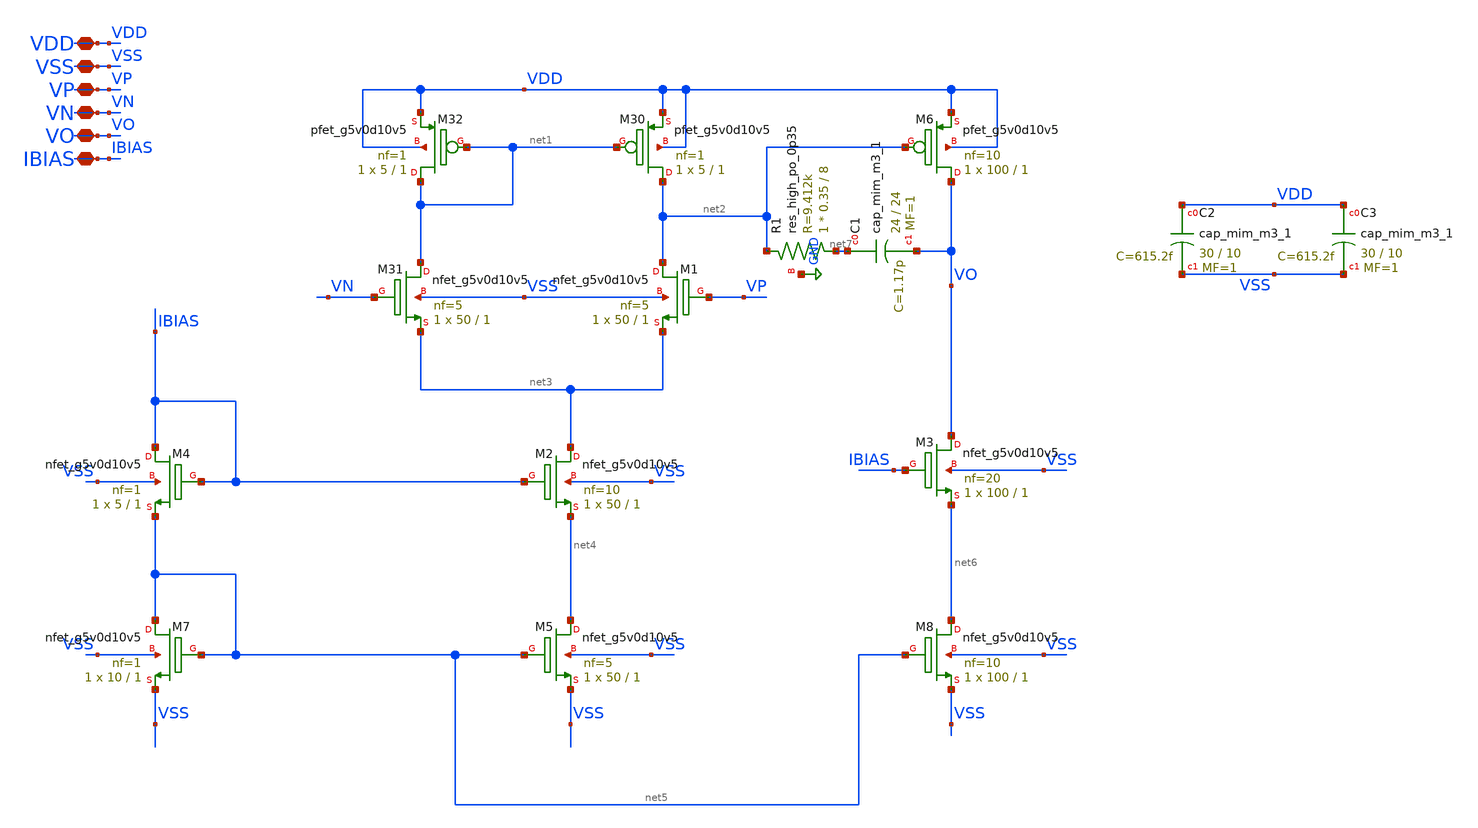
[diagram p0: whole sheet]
** sch_path: xschem/xschem_BGR_Top/Opamp_jaffar.sch
**.subckt Opamp_jaffar VDD VSS VP VN VO IBIAS
*.iopin VDD
*.iopin VSS
*.iopin VP
*.iopin VN
*.iopin VO
*.iopin IBIAS
XC1 net7 VO sky130_fd_pr__cap_mim_m3_1 W=24 L=24 MF=1 m=1
XC2 VDD VSS sky130_fd_pr__cap_mim_m3_1 W=30 L=10 MF=1 m=1
XC3 VDD VSS sky130_fd_pr__cap_mim_m3_1 W=30 L=10 MF=1 m=1
XM30 net2 net1 VDD VDD sky130_fd_pr__pfet_g5v0d10v5 L=1 W=5 nf=1 ad='int((nf+1)/2) * W/nf * 0.29' as='int((nf+2)/2) * W/nf * 0.29'
+ pd='2*int((nf+1)/2) * (W/nf + 0.29)' ps='2*int((nf+2)/2) * (W/nf + 0.29)' nrd='0.29 / W' nrs='0.29 / W'
+ sa=0 sb=0 sd=0 mult=1 m=1
XM32 net1 net1 VDD VDD sky130_fd_pr__pfet_g5v0d10v5 L=1 W=5 nf=1 ad='int((nf+1)/2) * W/nf * 0.29' as='int((nf+2)/2) * W/nf * 0.29'
+ pd='2*int((nf+1)/2) * (W/nf + 0.29)' ps='2*int((nf+2)/2) * (W/nf + 0.29)' nrd='0.29 / W' nrs='0.29 / W'
+ sa=0 sb=0 sd=0 mult=1 m=1
XM31 net1 VN net3 VSS sky130_fd_pr__nfet_g5v0d10v5 L=1 W=50 nf=5 ad='int((nf+1)/2) * W/nf * 0.29' as='int((nf+2)/2) * W/nf * 0.29'
+ pd='2*int((nf+1)/2) * (W/nf + 0.29)' ps='2*int((nf+2)/2) * (W/nf + 0.29)' nrd='0.29 / W' nrs='0.29 / W'
+ sa=0 sb=0 sd=0 mult=1 m=1
XM1 net2 VP net3 VSS sky130_fd_pr__nfet_g5v0d10v5 L=1 W=50 nf=5 ad='int((nf+1)/2) * W/nf * 0.29' as='int((nf+2)/2) * W/nf * 0.29'
+ pd='2*int((nf+1)/2) * (W/nf + 0.29)' ps='2*int((nf+2)/2) * (W/nf + 0.29)' nrd='0.29 / W' nrs='0.29 / W'
+ sa=0 sb=0 sd=0 mult=1 m=1
XM2 net3 IBIAS net4 VSS sky130_fd_pr__nfet_g5v0d10v5 L=1 W=50 nf=10 ad='int((nf+1)/2) * W/nf * 0.29'
+ as='int((nf+2)/2) * W/nf * 0.29' pd='2*int((nf+1)/2) * (W/nf + 0.29)' ps='2*int((nf+2)/2) * (W/nf + 0.29)'
+ nrd='0.29 / W' nrs='0.29 / W' sa=0 sb=0 sd=0 mult=1 m=1
XM3 VO IBIAS net6 VSS sky130_fd_pr__nfet_g5v0d10v5 L=1 W=100 nf=20 ad='int((nf+1)/2) * W/nf * 0.29' as='int((nf+2)/2) * W/nf * 0.29'
+ pd='2*int((nf+1)/2) * (W/nf + 0.29)' ps='2*int((nf+2)/2) * (W/nf + 0.29)' nrd='0.29 / W' nrs='0.29 / W'
+ sa=0 sb=0 sd=0 mult=1 m=1
XM4 IBIAS IBIAS net5 VSS sky130_fd_pr__nfet_g5v0d10v5 L=1 W=5 nf=1 ad='int((nf+1)/2) * W/nf * 0.29' as='int((nf+2)/2) * W/nf * 0.29'
+ pd='2*int((nf+1)/2) * (W/nf + 0.29)' ps='2*int((nf+2)/2) * (W/nf + 0.29)' nrd='0.29 / W' nrs='0.29 / W'
+ sa=0 sb=0 sd=0 mult=1 m=1
XM5 net4 net5 VSS VSS sky130_fd_pr__nfet_g5v0d10v5 L=1 W=50 nf=5 ad='int((nf+1)/2) * W/nf * 0.29' as='int((nf+2)/2) * W/nf * 0.29'
+ pd='2*int((nf+1)/2) * (W/nf + 0.29)' ps='2*int((nf+2)/2) * (W/nf + 0.29)' nrd='0.29 / W' nrs='0.29 / W'
+ sa=0 sb=0 sd=0 mult=1 m=1
XM7 net5 net5 VSS VSS sky130_fd_pr__nfet_g5v0d10v5 L=1 W=10 nf=1 ad='int((nf+1)/2) * W/nf * 0.29' as='int((nf+2)/2) * W/nf * 0.29'
+ pd='2*int((nf+1)/2) * (W/nf + 0.29)' ps='2*int((nf+2)/2) * (W/nf + 0.29)' nrd='0.29 / W' nrs='0.29 / W'
+ sa=0 sb=0 sd=0 mult=1 m=1
XM8 net6 net5 VSS VSS sky130_fd_pr__nfet_g5v0d10v5 L=1 W=100 nf=10 ad='int((nf+1)/2) * W/nf * 0.29' as='int((nf+2)/2) * W/nf * 0.29'
+ pd='2*int((nf+1)/2) * (W/nf + 0.29)' ps='2*int((nf+2)/2) * (W/nf + 0.29)' nrd='0.29 / W' nrs='0.29 / W'
+ sa=0 sb=0 sd=0 mult=1 m=1
XM6 VO net2 VDD VDD sky130_fd_pr__pfet_g5v0d10v5 L=1 W=100 nf=10 ad='int((nf+1)/2) * W/nf * 0.29' as='int((nf+2)/2) * W/nf * 0.29'
+ pd='2*int((nf+1)/2) * (W/nf + 0.29)' ps='2*int((nf+2)/2) * (W/nf + 0.29)' nrd='0.29 / W' nrs='0.29 / W'
+ sa=0 sb=0 sd=0 mult=1 m=1
XR1 net7 net2 GND sky130_fd_pr__res_high_po_0p35 L=8 mult=1 m=1
**.ends
.GLOBAL GND
.end
